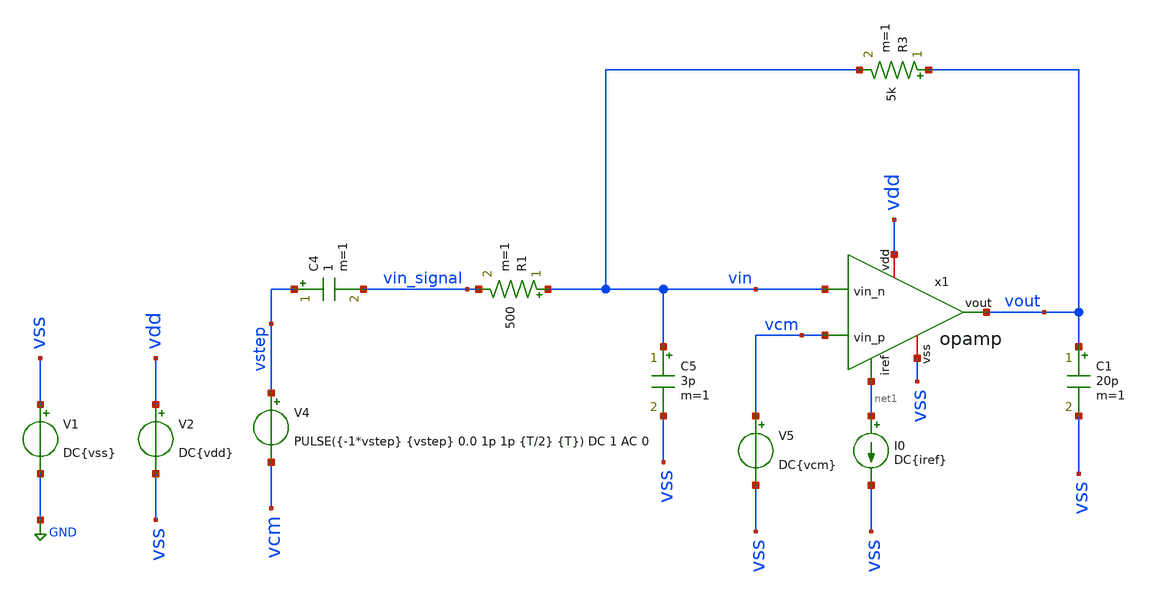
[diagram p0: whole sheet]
** sch_path: TpFinal/Mis Simulaciones/tb_opamp_stepresponse.sch
**.subckt tb_opamp_stepresponse
V1 vss GND DC{vss}
V2 vdd vss DC{vdd}
V4 vstep vcm PULSE({-1*vstep} {vstep} 0.0 1p 1p {T/2} {T}) DC 1 AC 0
C4 vstep vin_signal 1 m=1
I0 net1 vss DC{iref}
R1 vin vin_signal 500 m=1
R3 vout vin 5k m=1
C5 vin vss 3p m=1
C1 vout vss 20p m=1
V5 vcm vss DC{vcm}
x1 vdd net1 vin vcm vout vss opamp
**** begin user architecture code




* Circuit Parameters
.param iref = 100u
.param vdd  = 1.8
.param vss  = 0.0
.param vcm  = 0.8
.param vac  = 10m
.param vstep = 60m
.param T = 20u

.options TEMP = 65.0

* Include Models
.lib ~/skywater/skywater-pdk/libraries/sky130_fd_pr_ngspice/latest/models/corners/sky130.lib TT

* OP Parameters & Singals to save
.save all

*Simulations
.control
  set color0 = white

  tran 0.01u 20u
  setplot tran1
  plot v(vstep) v(vin_signal) v(vout)
.endc

.end


**** end user architecture code
**.ends

* expanding   symbol:  opamp.sym # of pins=6
** sym_path: opamp.sym
** sch_path: opamp.sch
.subckt opamp vdd iref vin_n vin_p vout vss
*.iopin vdd
*.iopin vss
*.ipin vin_n
*.ipin vin_p
*.ipin iref
*.opin vout
XM3 vbn vbn vss vss sky130_fd_pr__nfet_01v8 L=3.6 W=40 nf=1 ad='W * 0.29' as='W * 0.29' pd='2 * (W + 0.29)'
+ ps='2 * (W + 0.29)' nrd='0.29 / W' nrs='0.29 / W' sa=0 sb=0 sd=0 mult=17 m=17
XM4 voe1 vbn vss vss sky130_fd_pr__nfet_01v8 L=3.6 W=40 nf=1 ad='W * 0.29' as='W * 0.29' pd='2 * (W + 0.29)'
+ ps='2 * (W + 0.29)' nrd='0.29 / W' nrs='0.29 / W' sa=0 sb=0 sd=0 mult=17 m=17
XM5 vp iref vdd vdd sky130_fd_pr__pfet_01v8 L=0.8 W=60 nf=1 ad='W * 0.29' as='W * 0.29' pd='2 * (W + 0.29)'
+ ps='2 * (W + 0.29)' nrd='0.29 / W' nrs='0.29 / W' sa=0 sb=0 sd=0 mult=54 m=54
XM7 vout iref vdd vdd sky130_fd_pr__pfet_01v8 L=0.8 W=60 nf=1 ad='W * 0.29' as='W * 0.29' pd='2 * (W + 0.29)'
+ ps='2 * (W + 0.29)' nrd='0.29 / W' nrs='0.29 / W' sa=0 sb=0 sd=0 mult=68 m=68
XM8 iref iref vdd vdd sky130_fd_pr__pfet_01v8 L=0.8 W=60 nf=1 ad='W * 0.29' as='W * 0.29' pd='2 * (W + 0.29)'
+ ps='2 * (W + 0.29)' nrd='0.29 / W' nrs='0.29 / W' sa=0 sb=0 sd=0 mult=5 m=5
XM9 net1 vdd voe1 vss sky130_fd_pr__nfet_01v8 L=0.15 W=8.1 nf=1 ad='W * 0.29' as='W * 0.29' pd='2 * (W + 0.29)'
+ ps='2 * (W + 0.29)' nrd='0.29 / W' nrs='0.29 / W' sa=0 sb=0 sd=0 mult=1 m=1
XM6 vout voe1 vss vss sky130_fd_pr__nfet_01v8 L=0.16 W=82 nf=1 ad='W * 0.29' as='W * 0.29' pd='2 * (W + 0.29)'
+ ps='2 * (W + 0.29)' nrd='0.29 / W' nrs='0.29 / W' sa=0 sb=0 sd=0 mult=14 m=14
XM1 vbn vin_n vp vp sky130_fd_pr__pfet_01v8_lvt L=0.5 W=45 nf=1 ad='int((nf+1)/2) * W/nf * 0.29' as='int((nf+2)/2) * W/nf * 0.29'
+ pd='2*int((nf+1)/2) * (W/nf + 0.29)' ps='2*int((nf+2)/2) * (W/nf + 0.29)' nrd='0.29 / W' nrs='0.29 / W'
+ sa=0 sb=0 sd=0 mult=20 m=20
XM2 voe1 vin_p vp vp sky130_fd_pr__pfet_01v8_lvt L=0.5 W=45 nf=1 ad='int((nf+1)/2) * W/nf * 0.29' as='int((nf+2)/2) * W/nf * 0.29'
+ pd='2*int((nf+1)/2) * (W/nf + 0.29)' ps='2*int((nf+2)/2) * (W/nf + 0.29)' nrd='0.29 / W' nrs='0.29 / W'
+ sa=0 sb=0 sd=0 mult=20 m=20
C1 net1 vout 9.5p m=1
.ends

.GLOBAL GND
.end
